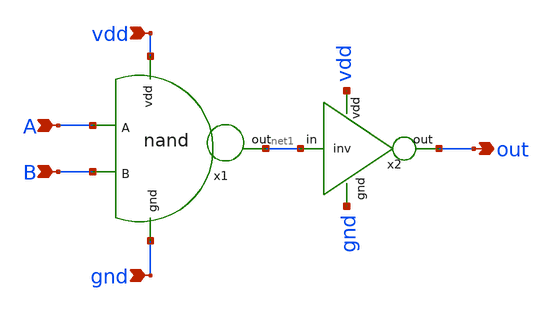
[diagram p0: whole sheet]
** sch_path: pll/dividers_lib/divider_design/and/xschem/and.sch
**.subckt and A B gnd vdd out
*.ipin A
*.ipin B
*.ipin gnd
*.ipin vdd
*.opin out
x1 vdd net1 A B gnd nand
x2 vdd net1 out gnd inv
**.ends
.end
